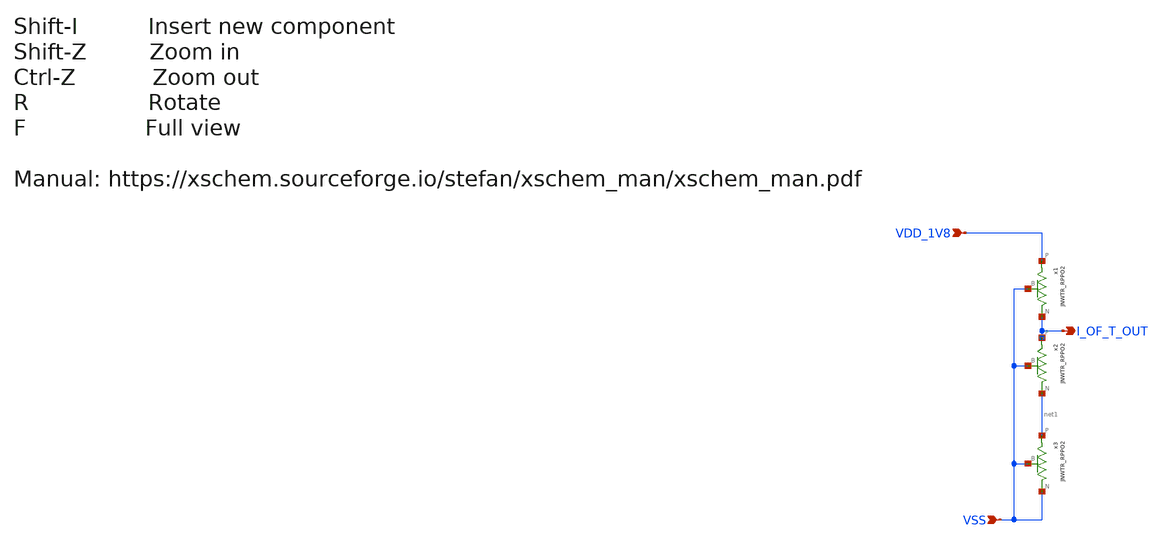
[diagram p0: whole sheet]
** sch_path: design/JNW_GR05_SKY130A/JNW_GR05.sch
**.subckt JNW_GR05 VDD_1V8 VSS I_OF_T_OUT
*.ipin VDD_1V8
*.ipin VSS
*.opin I_OF_T_OUT
x1 I_OF_T_OUT VDD_1V8 VSS JNWTR_RPPO2
x2 net1 I_OF_T_OUT VSS JNWTR_RPPO2
x3 VSS net1 VSS JNWTR_RPPO2
**.ends
.end
